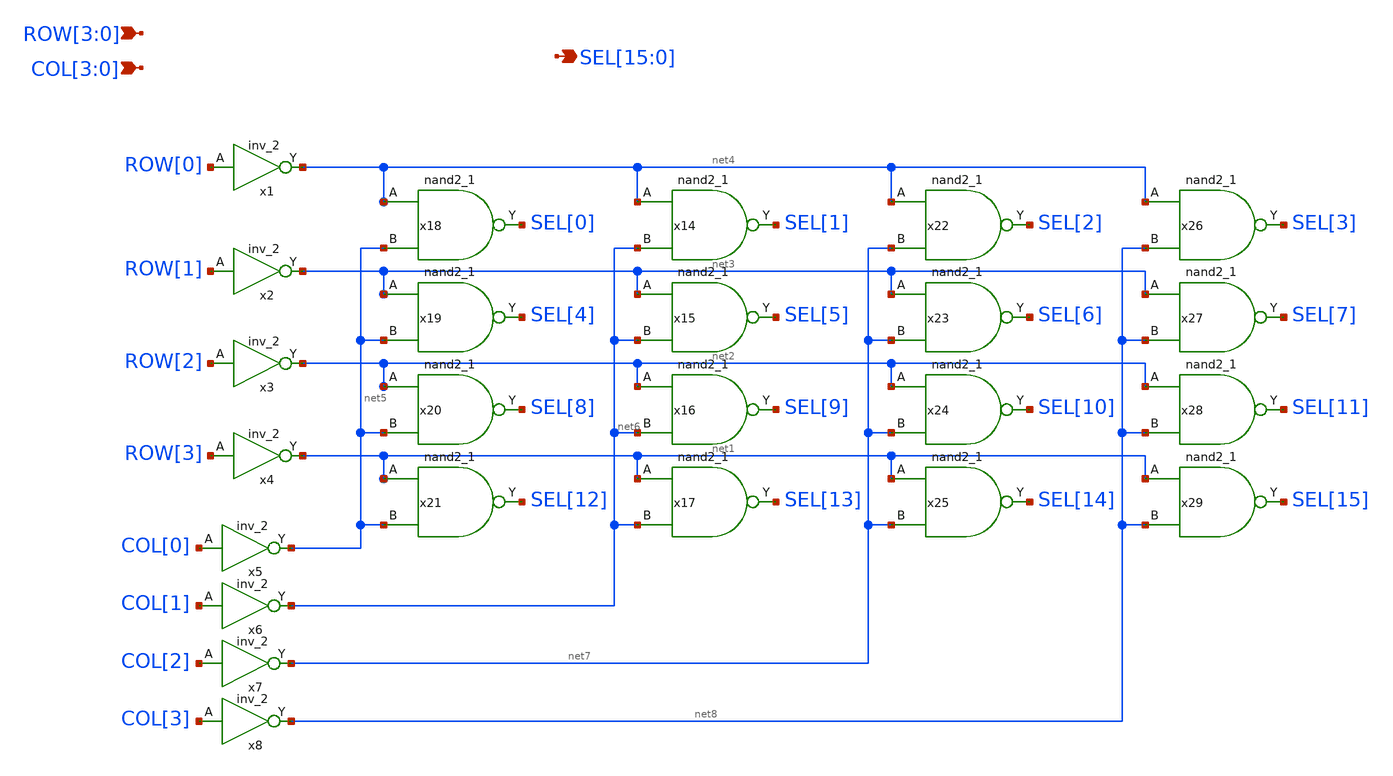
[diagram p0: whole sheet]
** sch_path: blocks/rom/rom_dec_cell.sch
**.subckt rom_dec_cell
*+ SEL[15],SEL[14],SEL[13],SEL[12],SEL[11],SEL[10],SEL[9],SEL[8],SEL[7],SEL[6],SEL[5],SEL[4],SEL[3],SEL[2],SEL[1],SEL[0] ROW[3],ROW[2],ROW[1],ROW[0] COL[3],COL[2],COL[1],COL[0]
*.opin
*+ SEL[15],SEL[14],SEL[13],SEL[12],SEL[11],SEL[10],SEL[9],SEL[8],SEL[7],SEL[6],SEL[5],SEL[4],SEL[3],SEL[2],SEL[1],SEL[0]
*.ipin ROW[3],ROW[2],ROW[1],ROW[0]
*.ipin COL[3],COL[2],COL[1],COL[0]
x2 ROW[1] VSS VSS VCC VCC net3 sky130_fd_sc_hs__inv_2
x3 ROW[2] VSS VSS VCC VCC net2 sky130_fd_sc_hs__inv_2
x4 ROW[3] VSS VSS VCC VCC net1 sky130_fd_sc_hs__inv_2
x5 COL[0] VSS VSS VCC VCC net5 sky130_fd_sc_hs__inv_2
x6 COL[1] VSS VSS VCC VCC net6 sky130_fd_sc_hs__inv_2
x7 COL[2] VSS VSS VCC VCC net7 sky130_fd_sc_hs__inv_2
x8 COL[3] VSS VSS VCC VCC net8 sky130_fd_sc_hs__inv_2
x1 ROW[0] VSS VSS VCC VCC net4 sky130_fd_sc_hs__inv_2
x14 net4 net6 VSS VSS VCC VCC SEL[1] sky130_fd_sc_hs__nand2_1
x15 net3 net6 VSS VSS VCC VCC SEL[5] sky130_fd_sc_hs__nand2_1
x16 net2 net6 VSS VSS VCC VCC SEL[9] sky130_fd_sc_hs__nand2_1
x17 net1 net6 VSS VSS VCC VCC SEL[13] sky130_fd_sc_hs__nand2_1
x18 net4 net5 VSS VSS VCC VCC SEL[0] sky130_fd_sc_hs__nand2_1
x19 net3 net5 VSS VSS VCC VCC SEL[4] sky130_fd_sc_hs__nand2_1
x20 net2 net5 VSS VSS VCC VCC SEL[8] sky130_fd_sc_hs__nand2_1
x21 net1 net5 VSS VSS VCC VCC SEL[12] sky130_fd_sc_hs__nand2_1
x22 net4 net7 VSS VSS VCC VCC SEL[2] sky130_fd_sc_hs__nand2_1
x23 net3 net7 VSS VSS VCC VCC SEL[6] sky130_fd_sc_hs__nand2_1
x24 net2 net7 VSS VSS VCC VCC SEL[10] sky130_fd_sc_hs__nand2_1
x25 net1 net7 VSS VSS VCC VCC SEL[14] sky130_fd_sc_hs__nand2_1
x26 net4 net8 VSS VSS VCC VCC SEL[3] sky130_fd_sc_hs__nand2_1
x27 net3 net8 VSS VSS VCC VCC SEL[7] sky130_fd_sc_hs__nand2_1
x28 net2 net8 VSS VSS VCC VCC SEL[11] sky130_fd_sc_hs__nand2_1
x29 net1 net8 VSS VSS VCC VCC SEL[15] sky130_fd_sc_hs__nand2_1
**.ends
.end
